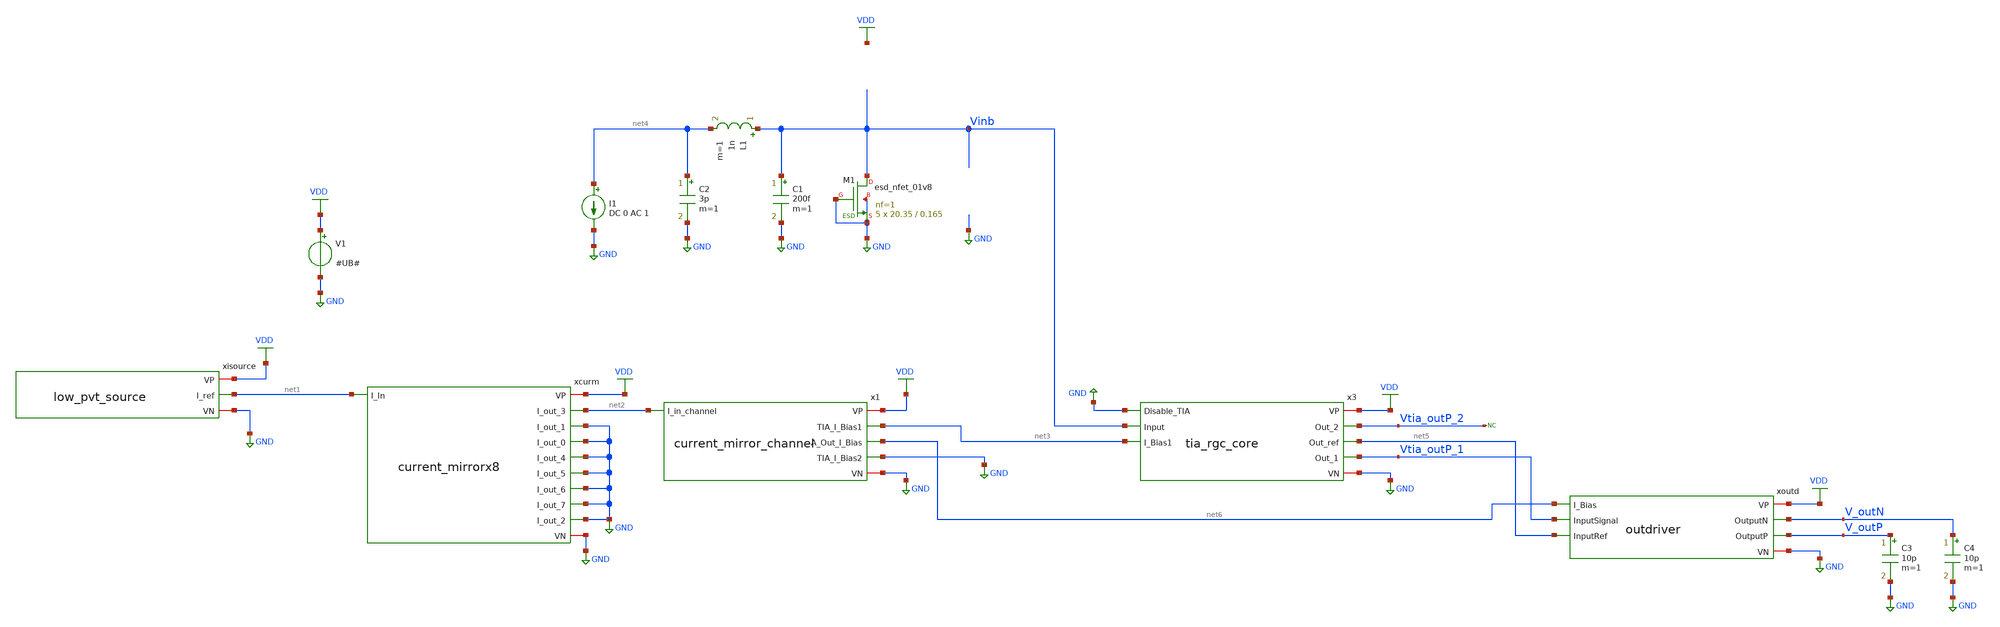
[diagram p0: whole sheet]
** sch_path: xschem/test/test_tia_rgc_integration_mc.sch
**.subckt test_tia_rgc_integration_mc
xcurm VDD net2 GND net1 GND GND GND GND GND GND GND current_mirrorx8
xisource VDD net1 GND low_pvt_source
x1 VDD net3 net6 GND net2 GND current_mirror_channel
V1 VDD GND #UB#
I1 net4 GND DC 0 AC 1
C1 Vinb GND 200f m=1
L1 Vinb net4 1n m=1
C2 net4 GND 3p m=1
XM1 Vinb GND GND GND sky130_fd_pr__esd_nfet_01v8 L=0.165 W=20.35 nf=1 ad='int((nf+1)/2) * W/nf * 0.29'
+ as='int((nf+2)/2) * W/nf * 0.29' pd='2*int((nf+1)/2) * (W/nf + 0.29)' ps='2*int((nf+2)/2) * (W/nf + 0.29)'
+ nrd='0.29 / W' nrs='0.29 / W' sa=0 sb=0 sd=0 mult=5 m=5
* noconn Vtia_outP_2
xoutd VDD V_outN V_outP net6 Vtia_outP_1 net5 GND outdriver
x3 VDD Vtia_outP_2 net5 Vtia_outP_1 GND Vinb net3 GND tia_rgc_core
C3 V_outP GND 10p m=1
C4 V_outN GND 10p m=1
**** begin user architecture code


*.options savecurrents
.option warn=1
* .option temp=100
.control
set wr_vecnames
set wr_singlescale
set hcopydevtype=svg

set model="#model#"
let mc_runs=3
let mc_runNo = 1

dowhile mc_runNo <= mc_runs
   destroy all
	let min_temp=0
	let var_temp = min_temp
	let max_temp=100
	let temp_step=30
	let noise_no=1
	dowhile var_temp <= max_temp
		op
		wrdata 'result_op_op_{$&var_temp}deg_{$&mc_runNo}.csv' v(v_outp) v(v_outn)

		* AC analysis
		ac dec 10 10 1T
		option temp=$&var_temp
		wrdata 'result_ac_ac_{$&var_temp}deg_{$&mc_runNo}.csv' v(vinb) vdb(vtia_outp_1) db(v(v_outp)-v(v_outn))

		* Measure AC at output driver
		meas ac gain_tia FIND vdb(vtia_outp_1) AT=10MEG
		meas ac max_gain_tia max vdb(vtia_outp_1) from=1MEG to=100G
		meas ac min_gain_tia min vdb(vtia_outp_1) from=1MEG to=100MEG
		let bw_gain_tia=gain_tia-3
		meas ac bandwidth_tia when vdb(vtia_outp_1)=bw_gain_tia fall = LAST
		wrdata result_meas_tia_{$&var_temp}deg_{$&mc_runNo}.csv gain_tia max_gain_tia min_gain_tia bandwidth_tia

		* Measure AC at output driver
		meas ac gain_out_p FIND vdb(v_outp) AT=10MEG
		meas ac gain_out_n FIND vdb(v_outn) AT=10MEG
		meas ac max_gain_out_p max vdb(v_outp) from=1MEG to=100G
		meas ac max_gain_out_n max vdb(v_outn) from=1MEG to=100G
		meas ac min_gain_out_n min vdb(v_outn) from=1MEG to=100MEG
		meas ac min_gain_out_p min vdb(v_outp) from=1MEG to=100MEG
		let bw_gain_out_p=gain_out_p-3
		let bw_gain_out_n=gain_out_n-3
		meas ac bandwidth_out_p when vdb(v_outp)=bw_gain_out_p fall = LAST
		meas ac bandwidth_out_n when vdb(v_outn)=bw_gain_out_n fall = LAST
		wrdata result_meas_out_{$&var_temp}deg_{$&mc_runNo}.csv gain_out_p gain_out_n max_gain_out_p max_gain_out_n
+ min_gain_out_n min_gain_out_p bandwidth_out_p bandwidth_out_n

		* noise at TIA
		noise v(vtia_outp_1) i1 dec 10 10 2G
		setplot noise1
		wrdata result_noise_tiaov_{$&var_temp}deg_{$&mc_runNo}.csv inoise_spectrum onoise_spectrum

		noise v(vtia_outp_1) i1 dec 10 2MEG 2G
		setplot noise3
		wrdata result_noise_tiazoom_{$&var_temp}deg_{$&mc_runNo}.csv inoise_spectrum onoise_spectrum

		noise v(v_outp) i1 dec 10 10 2G
		setplot noise5
		wrdata result_noise_outov_{$&var_temp}deg_{$&mc_runNo}.csv inoise_spectrum onoise_spectrum

		noise v(v_outp) i1 dec 10 2MEG 2G
		setplot noise7
		wrdata result_noise_outzoom_{$&var_temp}deg_{$&mc_runNo}.csv inoise_spectrum onoise_spectrum
		run
		let var_temp = var_temp + temp_step
	end
	let  mc_runNo = mc_runNo +1
	reset
end



.endc




* .include ../../tia.spice
* .include ../../filter_diff.spice
* .include ../../cmm_sense3.spice

.include ../../../tia_rgc_core.spice
.include ../../../current_mirror_channel.spice
.include ../../../current_mirrorx8.spice
.include ../../../low_pvt_source.spice
.include ../../../outdriver.spice



.lib $::SKYWATER_MODELS/sky130.lib.spice #model#
* .lib $::SKYWATER_MODELS/sky130.lib.spice sf
* .lib $::SKYWATER_MODELS/sky130.lib.spice.tt.red tt
* .lib /home/simon/share/pdk/sky130A/libs.tech/ngspice/sky130.lib.spice.tt.red tt

**** end user architecture code
**.ends

* expanding   symbol:  /home/simon/code/asic/analog/bias/current_mirrorx8.sym # of pins=11
** sym_path: xschem/bias/current_mirrorx8.sym
** sch_path: xschem/bias/current_mirrorx8.sch
.subckt current_mirrorx8 VP I_out_3 I_out_1 I_In I_out_0 I_out_4 I_out_5 I_out_6 I_out_7 I_out_2 VN
*.opin I_out_0
*.ipin I_In
*.iopin VP
*.opin I_out_1
*.opin I_out_2
*.opin I_out_3
*.opin I_out_4
*.opin I_out_5
*.opin I_out_6
*.opin I_out_7
*.iopin VN
XM1 net1 I_In VP VP sky130_fd_pr__pfet_01v8 L=1 W=2 nf=1 ad='int((nf+1)/2) * W/nf * 0.29' as='int((nf+2)/2) * W/nf * 0.29'
+ pd='2*int((nf+1)/2) * (W/nf + 0.29)' ps='2*int((nf+2)/2) * (W/nf + 0.29)' nrd='0.29 / W' nrs='0.29 / W'
+ sa=0 sb=0 sd=0 mult=4*4 m=4*4
XM2 I_In I_In net1 VP sky130_fd_pr__pfet_01v8 L=0.2 W=2 nf=1 ad='int((nf+1)/2) * W/nf * 0.29' as='int((nf+2)/2) * W/nf * 0.29'
+ pd='2*int((nf+1)/2) * (W/nf + 0.29)' ps='2*int((nf+2)/2) * (W/nf + 0.29)' nrd='0.29 / W' nrs='0.29 / W'
+ sa=0 sb=0 sd=0 mult=4 m=4
XC1 I_In VP sky130_fd_pr__cap_mim_m3_1 W=20 L=20 MF=1 m=1
XC2 VP I_In sky130_fd_pr__cap_mim_m3_2 W=20 L=20 MF=1 m=1
XC4 VP VN VN sky130_fd_pr__cap_var_lvt W=2 L=5 VM=5 m=5
XC3 I_In VN VN sky130_fd_pr__cap_var_lvt W=2 L=5 VM=5 m=5
XM3 net2 I_In VP VP sky130_fd_pr__pfet_01v8 L=1 W=2 nf=1 ad='int((nf+1)/2) * W/nf * 0.29' as='int((nf+2)/2) * W/nf * 0.29'
+ pd='2*int((nf+1)/2) * (W/nf + 0.29)' ps='2*int((nf+2)/2) * (W/nf + 0.29)' nrd='0.29 / W' nrs='0.29 / W'
+ sa=0 sb=0 sd=0 mult=4*4 m=4*4
XM4 I_out_0 I_In net2 VP sky130_fd_pr__pfet_01v8 L=0.2 W=2 nf=1 ad='int((nf+1)/2) * W/nf * 0.29' as='int((nf+2)/2) * W/nf * 0.29'
+ pd='2*int((nf+1)/2) * (W/nf + 0.29)' ps='2*int((nf+2)/2) * (W/nf + 0.29)' nrd='0.29 / W' nrs='0.29 / W'
+ sa=0 sb=0 sd=0 mult=4 m=4
XM5 net3 I_In VP VP sky130_fd_pr__pfet_01v8 L=1 W=2 nf=1 ad='int((nf+1)/2) * W/nf * 0.29' as='int((nf+2)/2) * W/nf * 0.29'
+ pd='2*int((nf+1)/2) * (W/nf + 0.29)' ps='2*int((nf+2)/2) * (W/nf + 0.29)' nrd='0.29 / W' nrs='0.29 / W'
+ sa=0 sb=0 sd=0 mult=4*4 m=4*4
XM6 I_out_1 I_In net3 VP sky130_fd_pr__pfet_01v8 L=0.2 W=2 nf=1 ad='int((nf+1)/2) * W/nf * 0.29' as='int((nf+2)/2) * W/nf * 0.29'
+ pd='2*int((nf+1)/2) * (W/nf + 0.29)' ps='2*int((nf+2)/2) * (W/nf + 0.29)' nrd='0.29 / W' nrs='0.29 / W'
+ sa=0 sb=0 sd=0 mult=4 m=4
XM7 net4 I_In VP VP sky130_fd_pr__pfet_01v8 L=1 W=2 nf=1 ad='int((nf+1)/2) * W/nf * 0.29' as='int((nf+2)/2) * W/nf * 0.29'
+ pd='2*int((nf+1)/2) * (W/nf + 0.29)' ps='2*int((nf+2)/2) * (W/nf + 0.29)' nrd='0.29 / W' nrs='0.29 / W'
+ sa=0 sb=0 sd=0 mult=4*4 m=4*4
XM8 I_out_2 I_In net4 VP sky130_fd_pr__pfet_01v8 L=0.2 W=2 nf=1 ad='int((nf+1)/2) * W/nf * 0.29' as='int((nf+2)/2) * W/nf * 0.29'
+ pd='2*int((nf+1)/2) * (W/nf + 0.29)' ps='2*int((nf+2)/2) * (W/nf + 0.29)' nrd='0.29 / W' nrs='0.29 / W'
+ sa=0 sb=0 sd=0 mult=4 m=4
XM9 net5 I_In VP VP sky130_fd_pr__pfet_01v8 L=1 W=2 nf=1 ad='int((nf+1)/2) * W/nf * 0.29' as='int((nf+2)/2) * W/nf * 0.29'
+ pd='2*int((nf+1)/2) * (W/nf + 0.29)' ps='2*int((nf+2)/2) * (W/nf + 0.29)' nrd='0.29 / W' nrs='0.29 / W'
+ sa=0 sb=0 sd=0 mult=4*4 m=4*4
XM10 I_out_3 I_In net5 VP sky130_fd_pr__pfet_01v8 L=0.2 W=2 nf=1 ad='int((nf+1)/2) * W/nf * 0.29' as='int((nf+2)/2) * W/nf * 0.29'
+ pd='2*int((nf+1)/2) * (W/nf + 0.29)' ps='2*int((nf+2)/2) * (W/nf + 0.29)' nrd='0.29 / W' nrs='0.29 / W'
+ sa=0 sb=0 sd=0 mult=4 m=4
XM11 net6 I_In VP VP sky130_fd_pr__pfet_01v8 L=1 W=2 nf=1 ad='int((nf+1)/2) * W/nf * 0.29' as='int((nf+2)/2) * W/nf * 0.29'
+ pd='2*int((nf+1)/2) * (W/nf + 0.29)' ps='2*int((nf+2)/2) * (W/nf + 0.29)' nrd='0.29 / W' nrs='0.29 / W'
+ sa=0 sb=0 sd=0 mult=4*4 m=4*4
XM12 I_out_4 I_In net6 VP sky130_fd_pr__pfet_01v8 L=0.2 W=2 nf=1 ad='int((nf+1)/2) * W/nf * 0.29' as='int((nf+2)/2) * W/nf * 0.29'
+ pd='2*int((nf+1)/2) * (W/nf + 0.29)' ps='2*int((nf+2)/2) * (W/nf + 0.29)' nrd='0.29 / W' nrs='0.29 / W'
+ sa=0 sb=0 sd=0 mult=4 m=4
XM13 net7 I_In VP VP sky130_fd_pr__pfet_01v8 L=1 W=2 nf=1 ad='int((nf+1)/2) * W/nf * 0.29' as='int((nf+2)/2) * W/nf * 0.29'
+ pd='2*int((nf+1)/2) * (W/nf + 0.29)' ps='2*int((nf+2)/2) * (W/nf + 0.29)' nrd='0.29 / W' nrs='0.29 / W'
+ sa=0 sb=0 sd=0 mult=4*4 m=4*4
XM14 I_out_5 I_In net7 VP sky130_fd_pr__pfet_01v8 L=0.2 W=2 nf=1 ad='int((nf+1)/2) * W/nf * 0.29' as='int((nf+2)/2) * W/nf * 0.29'
+ pd='2*int((nf+1)/2) * (W/nf + 0.29)' ps='2*int((nf+2)/2) * (W/nf + 0.29)' nrd='0.29 / W' nrs='0.29 / W'
+ sa=0 sb=0 sd=0 mult=4 m=4
XM15 net8 I_In VP VP sky130_fd_pr__pfet_01v8 L=1 W=2 nf=1 ad='int((nf+1)/2) * W/nf * 0.29' as='int((nf+2)/2) * W/nf * 0.29'
+ pd='2*int((nf+1)/2) * (W/nf + 0.29)' ps='2*int((nf+2)/2) * (W/nf + 0.29)' nrd='0.29 / W' nrs='0.29 / W'
+ sa=0 sb=0 sd=0 mult=4*4 m=4*4
XM16 I_out_6 I_In net8 VP sky130_fd_pr__pfet_01v8 L=0.2 W=2 nf=1 ad='int((nf+1)/2) * W/nf * 0.29' as='int((nf+2)/2) * W/nf * 0.29'
+ pd='2*int((nf+1)/2) * (W/nf + 0.29)' ps='2*int((nf+2)/2) * (W/nf + 0.29)' nrd='0.29 / W' nrs='0.29 / W'
+ sa=0 sb=0 sd=0 mult=4 m=4
XM17 net9 I_In VP VP sky130_fd_pr__pfet_01v8 L=1 W=2 nf=1 ad='int((nf+1)/2) * W/nf * 0.29' as='int((nf+2)/2) * W/nf * 0.29'
+ pd='2*int((nf+1)/2) * (W/nf + 0.29)' ps='2*int((nf+2)/2) * (W/nf + 0.29)' nrd='0.29 / W' nrs='0.29 / W'
+ sa=0 sb=0 sd=0 mult=4*4 m=4*4
XM18 I_out_7 I_In net9 VP sky130_fd_pr__pfet_01v8 L=0.2 W=2 nf=1 ad='int((nf+1)/2) * W/nf * 0.29' as='int((nf+2)/2) * W/nf * 0.29'
+ pd='2*int((nf+1)/2) * (W/nf + 0.29)' ps='2*int((nf+2)/2) * (W/nf + 0.29)' nrd='0.29 / W' nrs='0.29 / W'
+ sa=0 sb=0 sd=0 mult=4 m=4
.ends


* expanding   symbol:  /home/simon/code/asic/analog/bias/low_pvt_source.sym # of pins=3
** sym_path: xschem/bias/low_pvt_source.sym
** sch_path: xschem/bias/low_pvt_source.sch
.subckt low_pvt_source VP I_ref VN
*.iopin VP
*.opin I_ref
*.iopin VN
XM1 VM1D VM8D VP VP sky130_fd_pr__pfet_01v8 L=1 W=4 nf=1 ad='int((nf+1)/2) * W/nf * 0.29' as='int((nf+2)/2) * W/nf * 0.29'
+ pd='2*int((nf+1)/2) * (W/nf + 0.29)' ps='2*int((nf+2)/2) * (W/nf + 0.29)' nrd='0.29 / W' nrs='0.29 / W'
+ sa=0 sb=0 sd=0 mult=10 m=10
XM2 VM2D VM2D VN VN sky130_fd_pr__nfet_01v8 L=6 W=4 nf=1 ad='int((nf+1)/2) * W/nf * 0.29' as='int((nf+2)/2) * W/nf * 0.29'
+ pd='2*int((nf+1)/2) * (W/nf + 0.29)' ps='2*int((nf+2)/2) * (W/nf + 0.29)' nrd='0.29 / W' nrs='0.29 / W'
+ sa=0 sb=0 sd=0 mult=30 m=30
XM5 VM9D VM8D VM1D VP sky130_fd_pr__pfet_01v8 L=0.2 W=4 nf=1 ad='int((nf+1)/2) * W/nf * 0.29' as='int((nf+2)/2) * W/nf * 0.29'
+ pd='2*int((nf+1)/2) * (W/nf + 0.29)' ps='2*int((nf+2)/2) * (W/nf + 0.29)' nrd='0.29 / W' nrs='0.29 / W'
+ sa=0 sb=0 sd=0 mult=2 m=2
XM11 VM11D VM2D VM12D VN sky130_fd_pr__nfet_01v8 L=6 W=4 nf=1 ad='int((nf+1)/2) * W/nf * 0.29' as='int((nf+2)/2) * W/nf * 0.29'
+ pd='2*int((nf+1)/2) * (W/nf + 0.29)' ps='2*int((nf+2)/2) * (W/nf + 0.29)' nrd='0.29 / W' nrs='0.29 / W'
+ sa=0 sb=0 sd=0 mult=65 m=65
XM12 VM12D VM12G VN VN sky130_fd_pr__nfet_01v8 L=6 W=4 nf=1 ad='int((nf+1)/2) * W/nf * 0.29' as='int((nf+2)/2) * W/nf * 0.29'
+ pd='2*int((nf+1)/2) * (W/nf + 0.29)' ps='2*int((nf+2)/2) * (W/nf + 0.29)' nrd='0.29 / W' nrs='0.29 / W'
+ sa=0 sb=0 sd=0 mult=2 m=2
XM14 VM14D VM12G VN VN sky130_fd_pr__nfet_01v8 L=6 W=4 nf=1 ad='int((nf+1)/2) * W/nf * 0.29' as='int((nf+2)/2) * W/nf * 0.29'
+ pd='2*int((nf+1)/2) * (W/nf + 0.29)' ps='2*int((nf+2)/2) * (W/nf + 0.29)' nrd='0.29 / W' nrs='0.29 / W'
+ sa=0 sb=0 sd=0 mult=2 m=2
XM16 VM16D VM8D VP VP sky130_fd_pr__pfet_01v8 L=1 W=4 nf=1 ad='int((nf+1)/2) * W/nf * 0.29' as='int((nf+2)/2) * W/nf * 0.29'
+ pd='2*int((nf+1)/2) * (W/nf + 0.29)' ps='2*int((nf+2)/2) * (W/nf + 0.29)' nrd='0.29 / W' nrs='0.29 / W'
+ sa=0 sb=0 sd=0 mult=10 m=10
XM17 VM8D VM8D VM16D VP sky130_fd_pr__pfet_01v8 L=0.2 W=4 nf=1 ad='int((nf+1)/2) * W/nf * 0.29' as='int((nf+2)/2) * W/nf * 0.29'
+ pd='2*int((nf+1)/2) * (W/nf + 0.29)' ps='2*int((nf+2)/2) * (W/nf + 0.29)' nrd='0.29 / W' nrs='0.29 / W'
+ sa=0 sb=0 sd=0 mult=2 m=2
XM18 VM18D VM8D VP VP sky130_fd_pr__pfet_01v8 L=1 W=4 nf=1 ad='int((nf+1)/2) * W/nf * 0.29' as='int((nf+2)/2) * W/nf * 0.29'
+ pd='2*int((nf+1)/2) * (W/nf + 0.29)' ps='2*int((nf+2)/2) * (W/nf + 0.29)' nrd='0.29 / W' nrs='0.29 / W'
+ sa=0 sb=0 sd=0 mult=10*3*2 m=10*3*2
XM19 VM14D VM8D VM18D VP sky130_fd_pr__pfet_01v8 L=0.2 W=4 nf=1 ad='int((nf+1)/2) * W/nf * 0.29' as='int((nf+2)/2) * W/nf * 0.29'
+ pd='2*int((nf+1)/2) * (W/nf + 0.29)' ps='2*int((nf+2)/2) * (W/nf + 0.29)' nrd='0.29 / W' nrs='0.29 / W'
+ sa=0 sb=0 sd=0 mult=2*3*2 m=2*3*2
XM20 VM20D VM8D VP VP sky130_fd_pr__pfet_01v8 L=1 W=4 nf=1 ad='int((nf+1)/2) * W/nf * 0.29' as='int((nf+2)/2) * W/nf * 0.29'
+ pd='2*int((nf+1)/2) * (W/nf + 0.29)' ps='2*int((nf+2)/2) * (W/nf + 0.29)' nrd='0.29 / W' nrs='0.29 / W'
+ sa=0 sb=0 sd=0 mult=10*1*1 m=10*1*1
XM21 VM22D VM8D VM20D VP sky130_fd_pr__pfet_01v8 L=0.2 W=4 nf=1 ad='int((nf+1)/2) * W/nf * 0.29' as='int((nf+2)/2) * W/nf * 0.29'
+ pd='2*int((nf+1)/2) * (W/nf + 0.29)' ps='2*int((nf+2)/2) * (W/nf + 0.29)' nrd='0.29 / W' nrs='0.29 / W'
+ sa=0 sb=0 sd=0 mult=2*1*1 m=2*1*1
XM22 VM22D VM4S VM3D VN sky130_fd_pr__nfet_01v8 L=6 W=4 nf=1 ad='int((nf+1)/2) * W/nf * 0.29' as='int((nf+2)/2) * W/nf * 0.29'
+ pd='2*int((nf+1)/2) * (W/nf + 0.29)' ps='2*int((nf+2)/2) * (W/nf + 0.29)' nrd='0.29 / W' nrs='0.29 / W'
+ sa=0 sb=0 sd=0 mult=20 m=20
XM3 VM3D VM3G VN VN sky130_fd_pr__nfet_01v8 L=6 W=4 nf=1 ad='int((nf+1)/2) * W/nf * 0.29' as='int((nf+2)/2) * W/nf * 0.29'
+ pd='2*int((nf+1)/2) * (W/nf + 0.29)' ps='2*int((nf+2)/2) * (W/nf + 0.29)' nrd='0.29 / W' nrs='0.29 / W'
+ sa=0 sb=0 sd=0 mult=4 m=4
XM13 VP VM14D VM12G VM12G sky130_fd_pr__nfet_01v8_lvt L=0.15 W=4 nf=1 ad='int((nf+1)/2) * W/nf * 0.29'
+ as='int((nf+2)/2) * W/nf * 0.29' pd='2*int((nf+1)/2) * (W/nf + 0.29)' ps='2*int((nf+2)/2) * (W/nf + 0.29)'
+ nrd='0.29 / W' nrs='0.29 / W' sa=0 sb=0 sd=0 mult=20 m=20
XM4 I_ref VM22D VM4S VN sky130_fd_pr__nfet_01v8_lvt L=0.15 W=4 nf=1 ad='int((nf+1)/2) * W/nf * 0.29'
+ as='int((nf+2)/2) * W/nf * 0.29' pd='2*int((nf+1)/2) * (W/nf + 0.29)' ps='2*int((nf+2)/2) * (W/nf + 0.29)'
+ nrd='0.29 / W' nrs='0.29 / W' sa=0 sb=0 sd=0 mult=20 m=20
XM48 VM50D VM11D VP VP sky130_fd_pr__pfet_01v8 L=2 W=0.5 nf=1 ad='int((nf+1)/2) * W/nf * 0.29' as='int((nf+2)/2) * W/nf * 0.29'
+ pd='2*int((nf+1)/2) * (W/nf + 0.29)' ps='2*int((nf+2)/2) * (W/nf + 0.29)' nrd='0.29 / W' nrs='0.29 / W'
+ sa=0 sb=0 sd=0 mult=1 m=1
XM50 VM50D VM11D VN VN sky130_fd_pr__nfet_01v8_lvt L=0.2 W=4 nf=1 ad='int((nf+1)/2) * W/nf * 0.29' as='int((nf+2)/2) * W/nf * 0.29'
+ pd='2*int((nf+1)/2) * (W/nf + 0.29)' ps='2*int((nf+2)/2) * (W/nf + 0.29)' nrd='0.29 / W' nrs='0.29 / W'
+ sa=0 sb=0 sd=0 mult=10 m=10
XC3 VP VM8D sky130_fd_pr__cap_mim_m3_1 W=20 L=20 MF=1 m=1
XM8 VM8D VM9D VM11D VM11D sky130_fd_pr__nfet_01v8_lvt L=1 W=4 nf=1 ad='int((nf+1)/2) * W/nf * 0.29' as='int((nf+2)/2) * W/nf * 0.29'
+ pd='2*int((nf+1)/2) * (W/nf + 0.29)' ps='2*int((nf+2)/2) * (W/nf + 0.29)' nrd='0.29 / W' nrs='0.29 / W'
+ sa=0 sb=0 sd=0 mult=20 m=20
XM9 VM9D VM9D VM2D VM2D sky130_fd_pr__nfet_01v8_lvt L=1 W=4 nf=1 ad='int((nf+1)/2) * W/nf * 0.29' as='int((nf+2)/2) * W/nf * 0.29'
+ pd='2*int((nf+1)/2) * (W/nf + 0.29)' ps='2*int((nf+2)/2) * (W/nf + 0.29)' nrd='0.29 / W' nrs='0.29 / W'
+ sa=0 sb=0 sd=0 mult=20 m=20
XM10 VM8D VM50D VN VN sky130_fd_pr__nfet_01v8 L=2 W=0.5 nf=1 ad='int((nf+1)/2) * W/nf * 0.29' as='int((nf+2)/2) * W/nf * 0.29'
+ pd='2*int((nf+1)/2) * (W/nf + 0.29)' ps='2*int((nf+2)/2) * (W/nf + 0.29)' nrd='0.29 / W' nrs='0.29 / W'
+ sa=0 sb=0 sd=0 mult=1 m=1
XC4 VN VP sky130_fd_pr__cap_mim_m3_2 W=30 L=30 MF=1 m=1
XR7 net3 VM4S VN sky130_fd_pr__res_xhigh_po_1p41 L=10 mult=1 m=1
XR3 net4 net3 VN sky130_fd_pr__res_xhigh_po_1p41 L=10 mult=1 m=1
XR4 net2 net4 VN sky130_fd_pr__res_xhigh_po_1p41 L=10 mult=1 m=1
XR5 net1 net2 VN sky130_fd_pr__res_xhigh_po_1p41 L=10 mult=1 m=1
XR6 VN net1 VN sky130_fd_pr__res_xhigh_po_1p41 L=10 mult=1 m=1
XR8 net5 VM12G VN sky130_fd_pr__res_xhigh_po_1p41 L=10 mult=1 m=1
XR1 net5 VM3G VN sky130_fd_pr__res_xhigh_po_1p41 L=10 mult=1 m=1
XR2 net7 net6 VN sky130_fd_pr__res_xhigh_po_1p41 L=10 mult=1 m=1
XR9 VN net6 VN sky130_fd_pr__res_xhigh_po_1p41 L=10 mult=1 m=1
XR10 net11 net7 VN sky130_fd_pr__res_xhigh_po_1p41 L=10 mult=1 m=1
XR11 net12 net11 VN sky130_fd_pr__res_xhigh_po_1p41 L=10 mult=1 m=1
XR12 net8 net12 VN sky130_fd_pr__res_xhigh_po_1p41 L=10 mult=1 m=1
XR13 net10 VM3G VN sky130_fd_pr__res_xhigh_po_1p41 L=10 mult=1 m=1
XR14 net9 net10 VN sky130_fd_pr__res_xhigh_po_1p41 L=10 mult=1 m=1
XR15 net8 net9 VN sky130_fd_pr__res_xhigh_po_1p41 L=10 mult=1 m=1
XC1 VN VP sky130_fd_pr__cap_mim_m3_2 W=30 L=30 MF=1 m=1
.ends


* expanding   symbol:  /home/simon/code/asic/analog/bias/current_mirror_channel.sym # of pins=6
** sym_path: xschem/bias/current_mirror_channel.sym
** sch_path: xschem/bias/current_mirror_channel.sch
.subckt current_mirror_channel VP TIA_I_Bias1 A_Out_I_Bias TIA_I_Bias2 I_in_channel VN
*.ipin I_in_channel
*.iopin VP
*.opin TIA_I_Bias2
*.iopin VN
*.opin TIA_I_Bias1
*.opin A_Out_I_Bias
XM1 I_in_channel I_in_channel net1 VN sky130_fd_pr__nfet_01v8 L=0.2 W=2 nf=1 ad='int((nf+1)/2) * W/nf * 0.29'
+ as='int((nf+2)/2) * W/nf * 0.29' pd='2*int((nf+1)/2) * (W/nf + 0.29)' ps='2*int((nf+2)/2) * (W/nf + 0.29)'
+ nrd='0.29 / W' nrs='0.29 / W' sa=0 sb=0 sd=0 mult=2 m=2
XM2 net5 net4 VP VP sky130_fd_pr__pfet_01v8 L=1 W=2 nf=1 ad='int((nf+1)/2) * W/nf * 0.29' as='int((nf+2)/2) * W/nf * 0.29'
+ pd='2*int((nf+1)/2) * (W/nf + 0.29)' ps='2*int((nf+2)/2) * (W/nf + 0.29)' nrd='0.29 / W' nrs='0.29 / W'
+ sa=0 sb=0 sd=0 mult=4*4 m=4*4
XM3 net1 I_in_channel VN VN sky130_fd_pr__nfet_01v8 L=1 W=2 nf=1 ad='int((nf+1)/2) * W/nf * 0.29' as='int((nf+2)/2) * W/nf * 0.29'
+ pd='2*int((nf+1)/2) * (W/nf + 0.29)' ps='2*int((nf+2)/2) * (W/nf + 0.29)' nrd='0.29 / W' nrs='0.29 / W'
+ sa=0 sb=0 sd=0 mult=2*4 m=2*4
XM4 net4 net4 net5 VP sky130_fd_pr__pfet_01v8 L=0.2 W=2 nf=1 ad='int((nf+1)/2) * W/nf * 0.29' as='int((nf+2)/2) * W/nf * 0.29'
+ pd='2*int((nf+1)/2) * (W/nf + 0.29)' ps='2*int((nf+2)/2) * (W/nf + 0.29)' nrd='0.29 / W' nrs='0.29 / W'
+ sa=0 sb=0 sd=0 mult=4 m=4
XC8 net4 VP sky130_fd_pr__cap_mim_m3_2 W=30 L=30 MF=1 m=1
XM5 net4 I_in_channel net2 VN sky130_fd_pr__nfet_01v8 L=0.2 W=2 nf=1 ad='int((nf+1)/2) * W/nf * 0.29'
+ as='int((nf+2)/2) * W/nf * 0.29' pd='2*int((nf+1)/2) * (W/nf + 0.29)' ps='2*int((nf+2)/2) * (W/nf + 0.29)'
+ nrd='0.29 / W' nrs='0.29 / W' sa=0 sb=0 sd=0 mult=2 m=2
XM6 TIA_I_Bias2 I_in_channel net3 VN sky130_fd_pr__nfet_01v8 L=0.2 W=2 nf=1 ad='int((nf+1)/2) * W/nf * 0.29'
+ as='int((nf+2)/2) * W/nf * 0.29' pd='2*int((nf+1)/2) * (W/nf + 0.29)' ps='2*int((nf+2)/2) * (W/nf + 0.29)'
+ nrd='0.29 / W' nrs='0.29 / W' sa=0 sb=0 sd=0 mult=2 m=2
XM7 net2 I_in_channel VN VN sky130_fd_pr__nfet_01v8 L=1 W=2 nf=1 ad='int((nf+1)/2) * W/nf * 0.29' as='int((nf+2)/2) * W/nf * 0.29'
+ pd='2*int((nf+1)/2) * (W/nf + 0.29)' ps='2*int((nf+2)/2) * (W/nf + 0.29)' nrd='0.29 / W' nrs='0.29 / W'
+ sa=0 sb=0 sd=0 mult=2*4 m=2*4
XM8 net3 I_in_channel VN VN sky130_fd_pr__nfet_01v8 L=1 W=2 nf=1 ad='int((nf+1)/2) * W/nf * 0.29' as='int((nf+2)/2) * W/nf * 0.29'
+ pd='2*int((nf+1)/2) * (W/nf + 0.29)' ps='2*int((nf+2)/2) * (W/nf + 0.29)' nrd='0.29 / W' nrs='0.29 / W'
+ sa=0 sb=0 sd=0 mult=2*4 m=2*4
XM13 net6 net4 VP VP sky130_fd_pr__pfet_01v8 L=1 W=2 nf=1 ad='int((nf+1)/2) * W/nf * 0.29' as='int((nf+2)/2) * W/nf * 0.29'
+ pd='2*int((nf+1)/2) * (W/nf + 0.29)' ps='2*int((nf+2)/2) * (W/nf + 0.29)' nrd='0.29 / W' nrs='0.29 / W'
+ sa=0 sb=0 sd=0 mult=4*4*10 m=4*4*10
XM14 TIA_I_Bias1 net4 net6 VP sky130_fd_pr__pfet_01v8 L=0.2 W=2 nf=1 ad='int((nf+1)/2) * W/nf * 0.29'
+ as='int((nf+2)/2) * W/nf * 0.29' pd='2*int((nf+1)/2) * (W/nf + 0.29)' ps='2*int((nf+2)/2) * (W/nf + 0.29)'
+ nrd='0.29 / W' nrs='0.29 / W' sa=0 sb=0 sd=0 mult=4*10 m=4*10
XM9 net7 net4 VP VP sky130_fd_pr__pfet_01v8 L=1 W=2 nf=1 ad='int((nf+1)/2) * W/nf * 0.29' as='int((nf+2)/2) * W/nf * 0.29'
+ pd='2*int((nf+1)/2) * (W/nf + 0.29)' ps='2*int((nf+2)/2) * (W/nf + 0.29)' nrd='0.29 / W' nrs='0.29 / W'
+ sa=0 sb=0 sd=0 mult=4*4*12 m=4*4*12
XM10 A_Out_I_Bias net4 net7 VP sky130_fd_pr__pfet_01v8 L=0.2 W=2 nf=1 ad='int((nf+1)/2) * W/nf * 0.29'
+ as='int((nf+2)/2) * W/nf * 0.29' pd='2*int((nf+1)/2) * (W/nf + 0.29)' ps='2*int((nf+2)/2) * (W/nf + 0.29)'
+ nrd='0.29 / W' nrs='0.29 / W' sa=0 sb=0 sd=0 mult=4*12 m=4*12
XC4 net4 VP sky130_fd_pr__cap_mim_m3_2 W=30 L=30 MF=1 m=1
XC3 VN I_in_channel sky130_fd_pr__cap_mim_m3_2 W=30 L=30 MF=1 m=1
XC6 VN I_in_channel sky130_fd_pr__cap_mim_m3_2 W=30 L=30 MF=1 m=1
XC1 VN net4 sky130_fd_pr__cap_mim_m3_2 W=30 L=30 MF=1 m=1
XC2 VN VP sky130_fd_pr__cap_mim_m3_2 W=30 L=30 MF=1 m=1
.ends


* expanding   symbol:  /home/simon/code/asic/analog/outdriver/outdriver.sym # of pins=7
** sym_path: xschem/outdriver/outdriver.sym
** sch_path: xschem/outdriver/outdriver.sch
.subckt outdriver VP OutputN OutputP I_Bias InputSignal InputRef VN
*.iopin VN
*.ipin InputRef
*.iopin VP
*.ipin I_Bias
*.ipin InputSignal
*.opin OutputN
*.opin OutputP
XM1 V_da1_P InputSignal VM6D VM6D sky130_fd_pr__nfet_01v8_lvt L=0.15 W=2 nf=1 ad='int((nf+1)/2) * W/nf * 0.29'
+ as='int((nf+2)/2) * W/nf * 0.29' pd='2*int((nf+1)/2) * (W/nf + 0.29)' ps='2*int((nf+2)/2) * (W/nf + 0.29)'
+ nrd='0.29 / W' nrs='0.29 / W' sa=0 sb=0 sd=0 mult=11*2 m=11*2
XM3 VM3D I_Bias net4 VN sky130_fd_pr__nfet_01v8 L=0.5 W=2 nf=1 ad='int((nf+1)/2) * W/nf * 0.29' as='int((nf+2)/2) * W/nf * 0.29'
+ pd='2*int((nf+1)/2) * (W/nf + 0.29)' ps='2*int((nf+2)/2) * (W/nf + 0.29)' nrd='0.29 / W' nrs='0.29 / W'
+ sa=0 sb=0 sd=0 mult=2*(64) m=2*(64)
XM6 VM6D I_Bias VM3D VN sky130_fd_pr__nfet_01v8 L=0.15 W=2 nf=1 ad='int((nf+1)/2) * W/nf * 0.29' as='int((nf+2)/2) * W/nf * 0.29'
+ pd='2*int((nf+1)/2) * (W/nf + 0.29)' ps='2*int((nf+2)/2) * (W/nf + 0.29)' nrd='0.29 / W' nrs='0.29 / W'
+ sa=0 sb=0 sd=0 mult=64 m=64
XM7 I_Bias I_Bias net1 VN sky130_fd_pr__nfet_01v8 L=0.15 W=2 nf=1 ad='int((nf+1)/2) * W/nf * 0.29' as='int((nf+2)/2) * W/nf * 0.29'
+ pd='2*int((nf+1)/2) * (W/nf + 0.29)' ps='2*int((nf+2)/2) * (W/nf + 0.29)' nrd='0.29 / W' nrs='0.29 / W'
+ sa=0 sb=0 sd=0 mult=2 m=2
XM8 net1 I_Bias VN VN sky130_fd_pr__nfet_01v8 L=0.5 W=2 nf=1 ad='int((nf+1)/2) * W/nf * 0.29' as='int((nf+2)/2) * W/nf * 0.29'
+ pd='2*int((nf+1)/2) * (W/nf + 0.29)' ps='2*int((nf+2)/2) * (W/nf + 0.29)' nrd='0.29 / W' nrs='0.29 / W'
+ sa=0 sb=0 sd=0 mult=2*2 m=2*2
XM2 V_da2_P V_da1_P VM1_D VM1_D sky130_fd_pr__nfet_01v8_lvt L=0.15 W=2 nf=1 ad='int((nf+1)/2) * W/nf * 0.29'
+ as='int((nf+2)/2) * W/nf * 0.29' pd='2*int((nf+1)/2) * (W/nf + 0.29)' ps='2*int((nf+2)/2) * (W/nf + 0.29)'
+ nrd='0.29 / W' nrs='0.29 / W' sa=0 sb=0 sd=0 mult=44*2 m=44*2
XM4 V_da2_N V_da1_N VM1_D VM1_D sky130_fd_pr__nfet_01v8_lvt L=0.15 W=2 nf=1 ad='int((nf+1)/2) * W/nf * 0.29'
+ as='int((nf+2)/2) * W/nf * 0.29' pd='2*int((nf+1)/2) * (W/nf + 0.29)' ps='2*int((nf+2)/2) * (W/nf + 0.29)'
+ nrd='0.29 / W' nrs='0.29 / W' sa=0 sb=0 sd=0 mult=44*2 m=44*2
XM9 net2 I_Bias net5 VN sky130_fd_pr__nfet_01v8 L=0.5 W=2 nf=1 ad='int((nf+1)/2) * W/nf * 0.29' as='int((nf+2)/2) * W/nf * 0.29'
+ pd='2*int((nf+1)/2) * (W/nf + 0.29)' ps='2*int((nf+2)/2) * (W/nf + 0.29)' nrd='0.29 / W' nrs='0.29 / W'
+ sa=0 sb=0 sd=0 mult=2*(256+64) m=2*(256+64)
XM10 VM1_D I_Bias net2 VN sky130_fd_pr__nfet_01v8 L=0.15 W=2 nf=1 ad='int((nf+1)/2) * W/nf * 0.29' as='int((nf+2)/2) * W/nf * 0.29'
+ pd='2*int((nf+1)/2) * (W/nf + 0.29)' ps='2*int((nf+2)/2) * (W/nf + 0.29)' nrd='0.29 / W' nrs='0.29 / W'
+ sa=0 sb=0 sd=0 mult=256+64 m=256+64
XM11 OutputP V_da2_P VM14D VM14D sky130_fd_pr__nfet_01v8_lvt L=0.15 W=2 nf=1 ad='int((nf+1)/2) * W/nf * 0.29'
+ as='int((nf+2)/2) * W/nf * 0.29' pd='2*int((nf+1)/2) * (W/nf + 0.29)' ps='2*int((nf+2)/2) * (W/nf + 0.29)'
+ nrd='0.29 / W' nrs='0.29 / W' sa=0 sb=0 sd=0 mult=44*4*2 m=44*4*2
XM12 OutputN V_da2_N VM14D VM14D sky130_fd_pr__nfet_01v8_lvt L=0.15 W=2 nf=1 ad='int((nf+1)/2) * W/nf * 0.29'
+ as='int((nf+2)/2) * W/nf * 0.29' pd='2*int((nf+1)/2) * (W/nf + 0.29)' ps='2*int((nf+2)/2) * (W/nf + 0.29)'
+ nrd='0.29 / W' nrs='0.29 / W' sa=0 sb=0 sd=0 mult=44*4*2 m=44*4*2
XM13 net3 I_Bias net6 VN sky130_fd_pr__nfet_01v8 L=0.5 W=2 nf=1 ad='int((nf+1)/2) * W/nf * 0.29' as='int((nf+2)/2) * W/nf * 0.29'
+ pd='2*int((nf+1)/2) * (W/nf + 0.29)' ps='2*int((nf+2)/2) * (W/nf + 0.29)' nrd='0.29 / W' nrs='0.29 / W'
+ sa=0 sb=0 sd=0 mult=2*(1024+256) m=2*(1024+256)
XM14 VM14D I_Bias net3 VN sky130_fd_pr__nfet_01v8 L=0.15 W=2 nf=1 ad='int((nf+1)/2) * W/nf * 0.29' as='int((nf+2)/2) * W/nf * 0.29'
+ pd='2*int((nf+1)/2) * (W/nf + 0.29)' ps='2*int((nf+2)/2) * (W/nf + 0.29)' nrd='0.29 / W' nrs='0.29 / W'
+ sa=0 sb=0 sd=0 mult=1024+256 m=1024+256
XR7 V_da2_N VP VP sky130_fd_pr__res_high_po_5p73 L=4 mult=4*2 m=4*2
XR5 V_da2_P VP VP sky130_fd_pr__res_high_po_5p73 L=4 mult=4*2 m=4*2
XR3 V_da1_N VP VP sky130_fd_pr__res_high_po_2p85 L=6 mult=4 m=4
XR4 V_da1_P VP VP sky130_fd_pr__res_high_po_2p85 L=6 mult=4 m=4
XC2 InputRef VN sky130_fd_pr__cap_mim_m3_2 W=30 L=30 MF=1 m=1
XM5 V_da1_N InputRef VM6D VM6D sky130_fd_pr__nfet_01v8_lvt L=0.15 W=2 nf=1 ad='int((nf+1)/2) * W/nf * 0.29'
+ as='int((nf+2)/2) * W/nf * 0.29' pd='2*int((nf+1)/2) * (W/nf + 0.29)' ps='2*int((nf+2)/2) * (W/nf + 0.29)'
+ nrd='0.29 / W' nrs='0.29 / W' sa=0 sb=0 sd=0 mult=11*2 m=11*2
XR8 OutputP VP VP sky130_fd_pr__res_high_po_5p73 L=4 mult=16*2 m=16*2
XC1 InputRef VN sky130_fd_pr__cap_mim_m3_2 W=30 L=30 MF=1 m=1
XC6 VP VN sky130_fd_pr__cap_mim_m3_2 W=30 L=30 MF=1 m=1
XC8 VP VN sky130_fd_pr__cap_mim_m3_2 W=30 L=30 MF=1 m=1
V1 net4 VN 0
V2 net5 VN 0
V3 net6 VN 0
XR1 OutputN VP VP sky130_fd_pr__res_high_po_5p73 L=4 mult=16*2 m=16*2
XC7 VP VN sky130_fd_pr__cap_mim_m3_2 W=30 L=30 MF=1 m=1
XC9 VP VN sky130_fd_pr__cap_mim_m3_2 W=30 L=30 MF=1 m=1
XC10 VP VN sky130_fd_pr__cap_mim_m3_2 W=30 L=30 MF=1 m=1
XC11 VP VN sky130_fd_pr__cap_mim_m3_2 W=30 L=30 MF=1 m=1
XC12 VP VN sky130_fd_pr__cap_mim_m3_2 W=30 L=30 MF=1 m=1
XC13 VP VN sky130_fd_pr__cap_mim_m3_2 W=30 L=30 MF=1 m=1
XC14 VP VN sky130_fd_pr__cap_mim_m3_2 W=30 L=30 MF=1 m=1
XC5 I_Bias VN sky130_fd_pr__cap_mim_m3_1 W=20 L=20 MF=1 m=1
XC3 I_Bias VN sky130_fd_pr__cap_mim_m3_1 W=20 L=20 MF=1 m=1
.ends


* expanding   symbol:  /home/simon/code/asic/analog/tia/tia_rgc_core.sym # of pins=8
** sym_path: xschem/tia/tia_rgc_core.sym
** sch_path: xschem/tia/tia_rgc_core.sch
.subckt tia_rgc_core VP Out_2 Out_ref Out_1 Disable_TIA Input I_Bias1 VN
*.iopin VN
*.iopin VP
*.opin Out_2
*.ipin I_Bias1
*.ipin Input
*.ipin Disable_TIA
*.opin Out_1
*.opin Out_ref
XM5 VM5D I_Bias1 VN VN sky130_fd_pr__nfet_01v8 L=1 W=2 nf=1 ad='int((nf+1)/2) * W/nf * 0.29' as='int((nf+2)/2) * W/nf * 0.29'
+ pd='2*int((nf+1)/2) * (W/nf + 0.29)' ps='2*int((nf+2)/2) * (W/nf + 0.29)' nrd='0.29 / W' nrs='0.29 / W'
+ sa=0 sb=0 sd=0 mult=6 m=6
XM6 VM6D I_Bias1 VN VN sky130_fd_pr__nfet_01v8 L=1.0 W=2 nf=1 ad='int((nf+1)/2) * W/nf * 0.29' as='int((nf+2)/2) * W/nf * 0.29'
+ pd='2*int((nf+1)/2) * (W/nf + 0.29)' ps='2*int((nf+2)/2) * (W/nf + 0.29)' nrd='0.29 / W' nrs='0.29 / W'
+ sa=0 sb=0 sd=0 mult=6 m=6
XM7 Out_1 Input VM28D VN sky130_fd_pr__nfet_01v8_lvt L=0.2 W=2 nf=1 ad='int((nf+1)/2) * W/nf * 0.29'
+ as='int((nf+2)/2) * W/nf * 0.29' pd='2*int((nf+1)/2) * (W/nf + 0.29)' ps='2*int((nf+2)/2) * (W/nf + 0.29)'
+ nrd='0.29 / W' nrs='0.29 / W' sa=0 sb=0 sd=0 mult=100 m=100
XM8 Out_1 Input VP VP sky130_fd_pr__pfet_01v8 L=0.2 W=2 nf=1 ad='int((nf+1)/2) * W/nf * 0.29' as='int((nf+2)/2) * W/nf * 0.29'
+ pd='2*int((nf+1)/2) * (W/nf + 0.29)' ps='2*int((nf+2)/2) * (W/nf + 0.29)' nrd='0.29 / W' nrs='0.29 / W'
+ sa=0 sb=0 sd=0 mult=60 m=60
XM9 Input I_Bias1 VM5D VN sky130_fd_pr__nfet_01v8 L=0.15 W=2 nf=1 ad='int((nf+1)/2) * W/nf * 0.29' as='int((nf+2)/2) * W/nf * 0.29'
+ pd='2*int((nf+1)/2) * (W/nf + 0.29)' ps='2*int((nf+2)/2) * (W/nf + 0.29)' nrd='0.29 / W' nrs='0.29 / W'
+ sa=0 sb=0 sd=0 mult=12 m=12
XM10 I_Bias1 I_Bias1 VM6D VN sky130_fd_pr__nfet_01v8 L=0.15 W=2 nf=1 ad='int((nf+1)/2) * W/nf * 0.29'
+ as='int((nf+2)/2) * W/nf * 0.29' pd='2*int((nf+1)/2) * (W/nf + 0.29)' ps='2*int((nf+2)/2) * (W/nf + 0.29)'
+ nrd='0.29 / W' nrs='0.29 / W' sa=0 sb=0 sd=0 mult=12 m=12
XM23 I_Bias1 Disable_TIA VN VN sky130_fd_pr__nfet_01v8 L=0.15 W=2 nf=1 ad='int((nf+1)/2) * W/nf * 0.29'
+ as='int((nf+2)/2) * W/nf * 0.29' pd='2*int((nf+1)/2) * (W/nf + 0.29)' ps='2*int((nf+2)/2) * (W/nf + 0.29)'
+ nrd='0.29 / W' nrs='0.29 / W' sa=0 sb=0 sd=0 mult=5 m=5
XM26 Disable_TIA_B Disable_TIA VN VN sky130_fd_pr__nfet_01v8 L=1 W=0.5 nf=1 ad='int((nf+1)/2) * W/nf * 0.29'
+ as='int((nf+2)/2) * W/nf * 0.29' pd='2*int((nf+1)/2) * (W/nf + 0.29)' ps='2*int((nf+2)/2) * (W/nf + 0.29)'
+ nrd='0.29 / W' nrs='0.29 / W' sa=0 sb=0 sd=0 mult=1 m=1
XM27 Disable_TIA_B Disable_TIA VP VP sky130_fd_pr__pfet_01v8 L=1 W=0.5 nf=1 ad='int((nf+1)/2) * W/nf * 0.29'
+ as='int((nf+2)/2) * W/nf * 0.29' pd='2*int((nf+1)/2) * (W/nf + 0.29)' ps='2*int((nf+2)/2) * (W/nf + 0.29)'
+ nrd='0.29 / W' nrs='0.29 / W' sa=0 sb=0 sd=0 mult=1 m=1
XM28 VM28D Disable_TIA_B VN VN sky130_fd_pr__nfet_01v8 L=0.15 W=2 nf=1 ad='int((nf+1)/2) * W/nf * 0.29'
+ as='int((nf+2)/2) * W/nf * 0.29' pd='2*int((nf+1)/2) * (W/nf + 0.29)' ps='2*int((nf+2)/2) * (W/nf + 0.29)'
+ nrd='0.29 / W' nrs='0.29 / W' sa=0 sb=0 sd=0 mult=100 m=100
XM36 VM36D I_Bias1 VN VN sky130_fd_pr__nfet_01v8 L=1 W=2 nf=1 ad='int((nf+1)/2) * W/nf * 0.29' as='int((nf+2)/2) * W/nf * 0.29'
+ pd='2*int((nf+1)/2) * (W/nf + 0.29)' ps='2*int((nf+2)/2) * (W/nf + 0.29)' nrd='0.29 / W' nrs='0.29 / W'
+ sa=0 sb=0 sd=0 mult=6 m=6
XM37 Out_ref VM39D VM40D VN sky130_fd_pr__nfet_01v8_lvt L=0.2 W=2 nf=1 ad='int((nf+1)/2) * W/nf * 0.29'
+ as='int((nf+2)/2) * W/nf * 0.29' pd='2*int((nf+1)/2) * (W/nf + 0.29)' ps='2*int((nf+2)/2) * (W/nf + 0.29)'
+ nrd='0.29 / W' nrs='0.29 / W' sa=0 sb=0 sd=0 mult=100 m=100
XM38 Out_ref VM39D VP VP sky130_fd_pr__pfet_01v8 L=0.2 W=2 nf=1 ad='int((nf+1)/2) * W/nf * 0.29' as='int((nf+2)/2) * W/nf * 0.29'
+ pd='2*int((nf+1)/2) * (W/nf + 0.29)' ps='2*int((nf+2)/2) * (W/nf + 0.29)' nrd='0.29 / W' nrs='0.29 / W'
+ sa=0 sb=0 sd=0 mult=60 m=60
XM39 VM39D I_Bias1 VM36D VN sky130_fd_pr__nfet_01v8 L=0.15 W=2 nf=1 ad='int((nf+1)/2) * W/nf * 0.29'
+ as='int((nf+2)/2) * W/nf * 0.29' pd='2*int((nf+1)/2) * (W/nf + 0.29)' ps='2*int((nf+2)/2) * (W/nf + 0.29)'
+ nrd='0.29 / W' nrs='0.29 / W' sa=0 sb=0 sd=0 mult=12 m=12
XM40 VM40D Disable_TIA_B VN VN sky130_fd_pr__nfet_01v8 L=0.15 W=2 nf=1 ad='int((nf+1)/2) * W/nf * 0.29'
+ as='int((nf+2)/2) * W/nf * 0.29' pd='2*int((nf+1)/2) * (W/nf + 0.29)' ps='2*int((nf+2)/2) * (W/nf + 0.29)'
+ nrd='0.29 / W' nrs='0.29 / W' sa=0 sb=0 sd=0 mult=100 m=100
XC20 VP VN sky130_fd_pr__cap_mim_m3_2 W=30 L=30 MF=1 m=1
XM16 Out_2 VN VP VP sky130_fd_pr__pfet_01v8 L=0.5 W=2 nf=1 ad='int((nf+1)/2) * W/nf * 0.29' as='int((nf+2)/2) * W/nf * 0.29'
+ pd='2*int((nf+1)/2) * (W/nf + 0.29)' ps='2*int((nf+2)/2) * (W/nf + 0.29)' nrd='0.29 / W' nrs='0.29 / W'
+ sa=0 sb=0 sd=0 mult=10 m=10
XM15 Out_2 Out_1 Input Input sky130_fd_pr__nfet_01v8_lvt L=0.2 W=2 nf=1 ad='int((nf+1)/2) * W/nf * 0.29'
+ as='int((nf+2)/2) * W/nf * 0.29' pd='2*int((nf+1)/2) * (W/nf + 0.29)' ps='2*int((nf+2)/2) * (W/nf + 0.29)'
+ nrd='0.29 / W' nrs='0.29 / W' sa=0 sb=0 sd=0 mult=30 m=30
XM31 VM31D Out_ref VM39D VM39D sky130_fd_pr__nfet_01v8_lvt L=0.2 W=2 nf=1 ad='int((nf+1)/2) * W/nf * 0.29'
+ as='int((nf+2)/2) * W/nf * 0.29' pd='2*int((nf+1)/2) * (W/nf + 0.29)' ps='2*int((nf+2)/2) * (W/nf + 0.29)'
+ nrd='0.29 / W' nrs='0.29 / W' sa=0 sb=0 sd=0 mult=30 m=30
XM35 VM31D VN VP VP sky130_fd_pr__pfet_01v8 L=0.5 W=2 nf=1 ad='int((nf+1)/2) * W/nf * 0.29' as='int((nf+2)/2) * W/nf * 0.29'
+ pd='2*int((nf+1)/2) * (W/nf + 0.29)' ps='2*int((nf+2)/2) * (W/nf + 0.29)' nrd='0.29 / W' nrs='0.29 / W'
+ sa=0 sb=0 sd=0 mult=10 m=10
XC7 VP VN sky130_fd_pr__cap_mim_m3_2 W=30 L=30 MF=1 m=1
XC2 VP VM28D sky130_fd_pr__cap_mim_m3_2 W=20 L=30 MF=1 m=1
XC5 VN I_Bias1 sky130_fd_pr__cap_mim_m3_1 W=15 L=12 MF=1 m=1
XC4 VN I_Bias1 sky130_fd_pr__cap_mim_m3_1 W=15 L=12 MF=1 m=1
XC1 VP VM40D sky130_fd_pr__cap_mim_m3_2 W=20 L=30 MF=1 m=1
XC3 Disable_TIA_B VN VN sky130_fd_pr__cap_var_lvt W=2 L=5 VM=5 m=5
.ends

.GLOBAL GND
.GLOBAL VDD
.end
